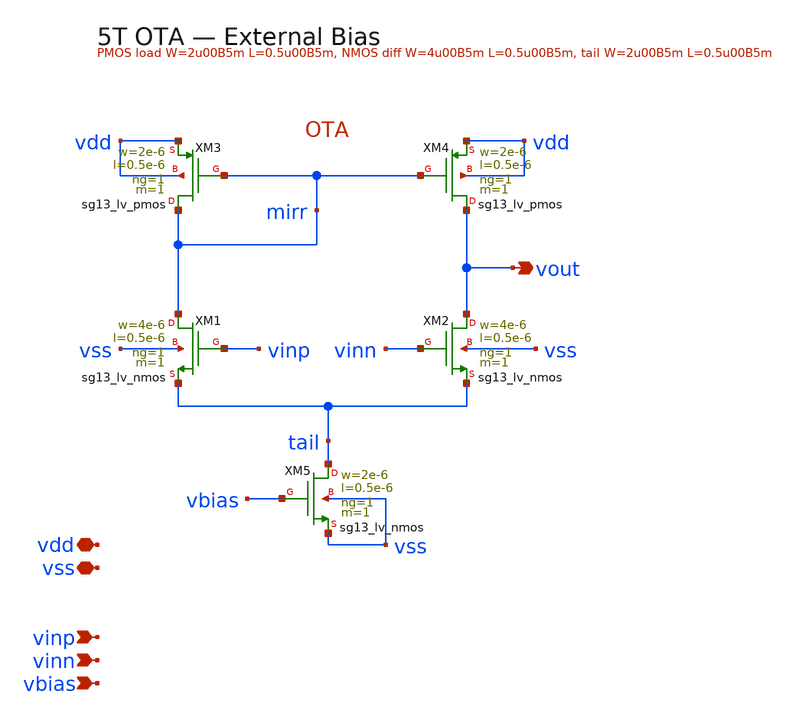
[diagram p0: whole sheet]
** sch_path: xschem/svf_ota5t.sch
**.subckt svf_ota5t vdd vss vinp vinn vout vbias
*.iopin vdd
*.iopin vss
*.ipin vinp
*.ipin vinn
*.opin vout
*.ipin vbias
XXM3 mirr mirr vdd vdd sg13_lv_pmos w=2e-6 l=0.5e-6 ng=1 m=1 mm_ok=1
XXM4 vout mirr vdd vdd sg13_lv_pmos w=2e-6 l=0.5e-6 ng=1 m=1 mm_ok=1
XXM1 mirr vinp tail vss sg13_lv_nmos w=4e-6 l=0.5e-6 ng=1 m=1 mm_ok=1
XXM2 vout vinn tail vss sg13_lv_nmos w=4e-6 l=0.5e-6 ng=1 m=1 mm_ok=1
XXM5 tail vbias vss vss sg13_lv_nmos w=2e-6 l=0.5e-6 ng=1 m=1 mm_ok=1
**.ends
.end
